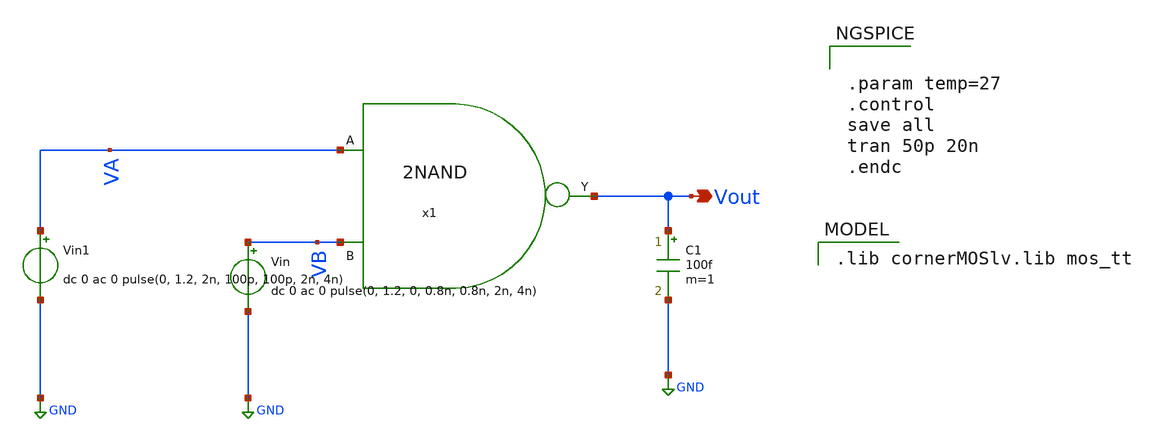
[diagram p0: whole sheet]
** sch_path: Team 1 Design/design_data/xschem/2_Input_NAND/2NAND_tb.sch
**.subckt 2NAND_tb Vout
*.opin Vout
x1 VA Vout VB 2NAND
Vin VB GND dc 0 ac 0 pulse(0, 1.2, 0, 0.8n, 0.8n, 2n, 4n)
Vin1 VA GND dc 0 ac 0 pulse(0, 1.2, 2n, 100p, 100p, 2n, 4n)
C1 Vout GND 100f m=1
**** begin user architecture code
 .lib cornerMOSlv.lib mos_tt



.param temp=27
.control
save all
tran 50p 20n
.endc


**** end user architecture code
**.ends

* expanding   symbol:  /foss/designs/Team2/2NAND/2NAND.sym # of pins=3
** sym_path: Team 1 Design/design_data/xschem/2_Input_NAND/2NAND.sym
** sch_path: Team 1 Design/design_data/xschem/2_Input_NAND/2NAND.sch
.subckt 2NAND A Y B
*.ipin B
*.opin Y
*.ipin A
XM1 Y A net1 net1 sg13_lv_pmos w=2u l=0.13u ng=1 m=1 mm_ok=1
XM2 Y B net1 net1 sg13_lv_pmos w=2u l=0.13u ng=1 m=1 mm_ok=1
XM3 Y B net2 GND sg13_lv_nmos w=1u l=0.13u ng=1 m=1 mm_ok=1
XM4 net2 A GND GND sg13_lv_nmos w=1u l=0.13u ng=1 m=1 mm_ok=1
V1 net1 GND 1.2
.ends

.GLOBAL GND
.end
